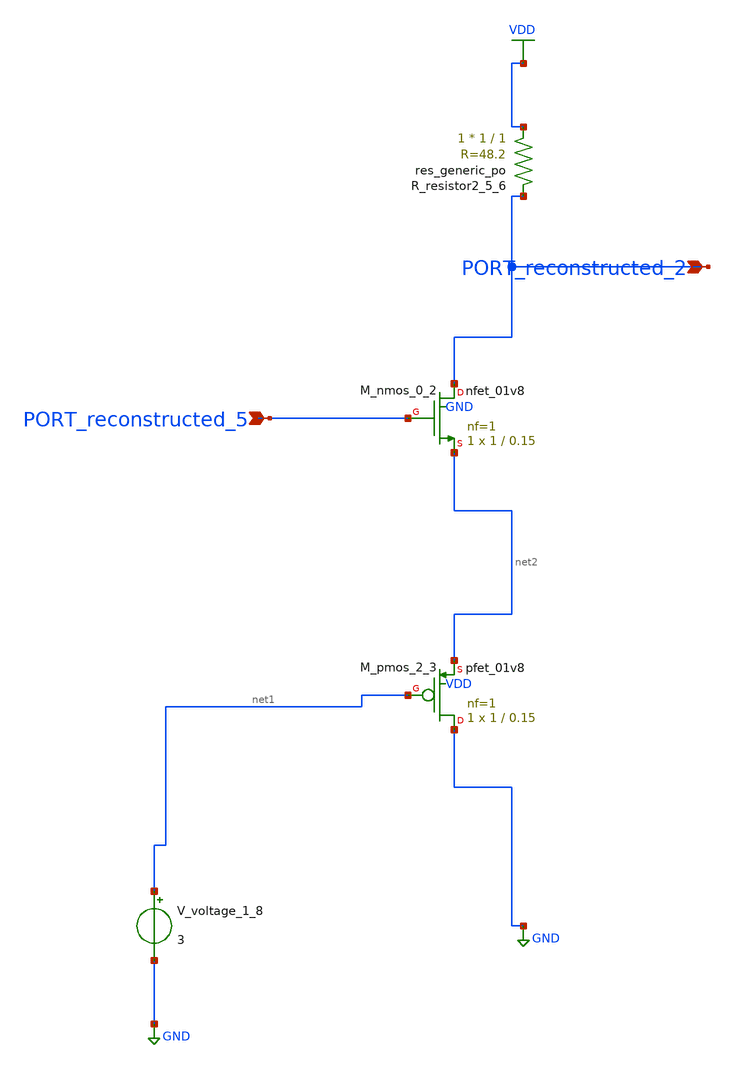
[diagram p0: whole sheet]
** sch_path: schematics/AMSNet/115.sch
**.subckt 115 PORT_reconstructed_5 PORT_reconstructed_2
*.ipin PORT_reconstructed_5
*.ipin PORT_reconstructed_2
XM_nmos_0_2 PORT_reconstructed_2 PORT_reconstructed_5 net2 GND sky130_fd_pr__nfet_01v8 L=0.15 W=1 nf=1
+ ad='int((1 + 1)/2) * 1 / 1 * 0.29' as='int((1 + 2)/2) * 1 / 1 * 0.29' pd='2*int((1 + 1)/2) * (1 / 1 + 0.29)'
+ ps='2*int((1 + 2)/2) * (1 / 1 + 0.29)' nrd='0.29 / 1 ' nrs='0.29 / 1 ' sa=0 sb=0 sd=0 mult=1 m=1
XM_pmos_2_3 GND net1 net2 VDD sky130_fd_pr__pfet_01v8 L=0.15 W=1 nf=1 ad='int((1 + 1)/2) * 1 / 1 * 0.29'
+ as='int((1 + 2)/2) * 1 / 1 * 0.29' pd='2*int((1 + 1)/2) * (1 / 1 + 0.29)' ps='2*int((1 + 2)/2) * (1 / 1 + 0.29)'
+ nrd='0.29 / 1 ' nrs='0.29 / 1 ' sa=0 sb=0 sd=0 mult=1 m=1
XR_resistor2_5_6 VDD PORT_reconstructed_2 sky130_fd_pr__res_generic_po W=1 L=1 m=1
V_voltage_1_8 net1 GND 3
**.ends
.GLOBAL GND
.GLOBAL VDD
.end
